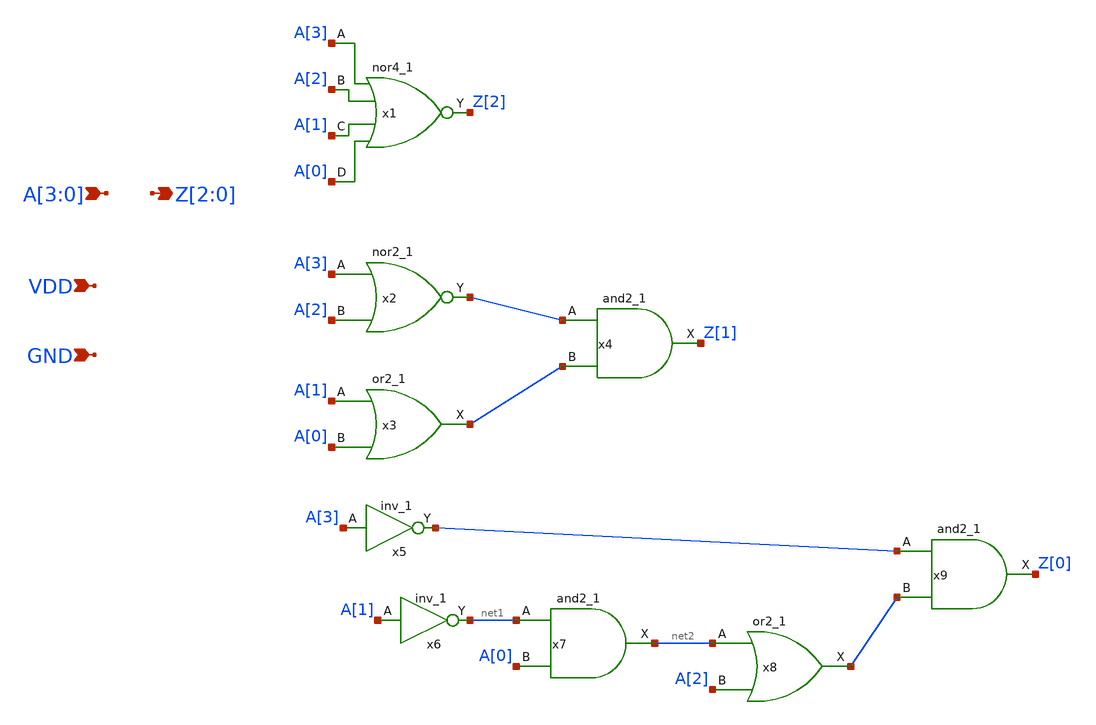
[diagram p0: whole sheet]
** sch_path: xschem/zlc_4bit.sch
**.subckt zlc_4bit A[3],A[2],A[1],A[0] Z[2],Z[1],Z[0] VDD GND
*.ipin A[3],A[2],A[1],A[0]
*.opin Z[2],Z[1],Z[0]
*.ipin VDD
*.ipin GND
x1 A[3] A[2] A[1] A[0] GND GND VDD VDD Z[2] sky130_fd_sc_hd__nor4_1
x2 A[3] A[2] GND GND VDD VDD net5 sky130_fd_sc_hd__nor2_1
x3 A[1] A[0] GND GND VDD VDD net6 sky130_fd_sc_hd__or2_1
x4 net5 net6 GND GND VDD VDD Z[1] sky130_fd_sc_hd__and2_1
x5 A[3] GND GND VDD VDD net4 sky130_fd_sc_hd__inv_1
x7 net1 A[0] GND GND VDD VDD net2 sky130_fd_sc_hd__and2_1
x8 net2 A[2] GND GND VDD VDD net3 sky130_fd_sc_hd__or2_1
x9 net4 net3 GND GND VDD VDD Z[0] sky130_fd_sc_hd__and2_1
x6 A[1] GND GND VDD VDD net1 sky130_fd_sc_hd__inv_1
**.ends
.end
